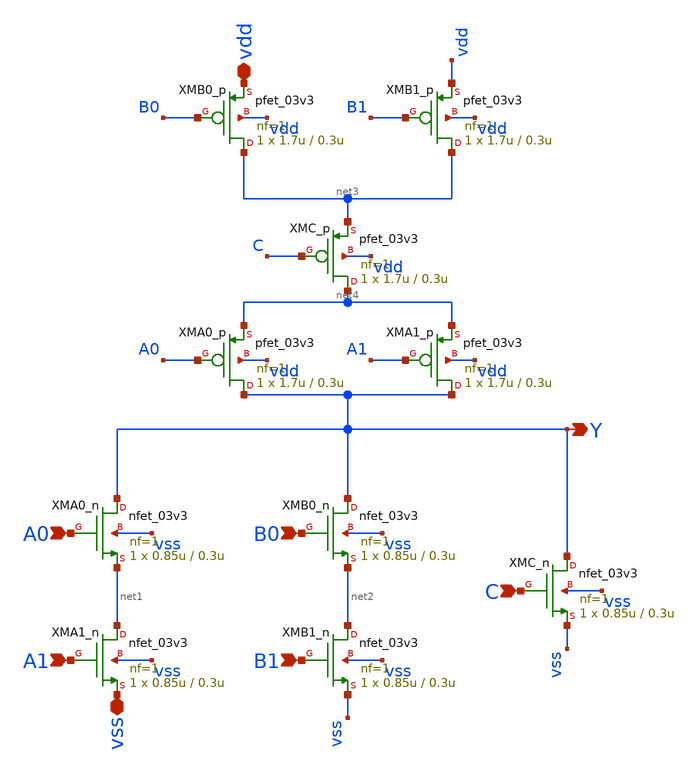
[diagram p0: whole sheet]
** sch_path: gf180mcu_osu_sc_gp9t3v3/xschem/gf180mcu_osu_sc_gp9t3v3__aoi221_1.sch
**.subckt gf180mcu_osu_sc_gp9t3v3__aoi221_1 vdd vss A0 A1 B1 B0 C Y
*.iopin vdd
*.iopin vss
*.ipin A0
*.ipin A1
*.ipin B1
*.ipin B0
*.ipin C
*.opin Y
XMA0_n Y A0 net1 vss nfet_03v3 L=0.3u W=0.85u nf=1 ad='int((nf+1)/2) * W/nf * 0.18u' as='int((nf+2)/2) * W/nf * 0.18u'
+ pd='2*int((nf+1)/2) * (W/nf + 0.18u)' ps='2*int((nf+2)/2) * (W/nf + 0.18u)' nrd='0.18u / W' nrs='0.18u / W'
+ sa=0 sb=0 sd=0 m=1
XMA1_n net1 A1 vss vss nfet_03v3 L=0.3u W=0.85u nf=1 ad='int((nf+1)/2) * W/nf * 0.18u' as='int((nf+2)/2) * W/nf * 0.18u'
+ pd='2*int((nf+1)/2) * (W/nf + 0.18u)' ps='2*int((nf+2)/2) * (W/nf + 0.18u)' nrd='0.18u / W' nrs='0.18u / W'
+ sa=0 sb=0 sd=0 m=1
XMB0_n Y B0 net2 vss nfet_03v3 L=0.3u W=0.85u nf=1 ad='int((nf+1)/2) * W/nf * 0.18u' as='int((nf+2)/2) * W/nf * 0.18u'
+ pd='2*int((nf+1)/2) * (W/nf + 0.18u)' ps='2*int((nf+2)/2) * (W/nf + 0.18u)' nrd='0.18u / W' nrs='0.18u / W'
+ sa=0 sb=0 sd=0 m=1
XMB1_n net2 B1 vss vss nfet_03v3 L=0.3u W=0.85u nf=1 ad='int((nf+1)/2) * W/nf * 0.18u' as='int((nf+2)/2) * W/nf * 0.18u'
+ pd='2*int((nf+1)/2) * (W/nf + 0.18u)' ps='2*int((nf+2)/2) * (W/nf + 0.18u)' nrd='0.18u / W' nrs='0.18u / W'
+ sa=0 sb=0 sd=0 m=1
XMC_n Y C vss vss nfet_03v3 L=0.3u W=0.85u nf=1 ad='int((nf+1)/2) * W/nf * 0.18u' as='int((nf+2)/2) * W/nf * 0.18u'
+ pd='2*int((nf+1)/2) * (W/nf + 0.18u)' ps='2*int((nf+2)/2) * (W/nf + 0.18u)' nrd='0.18u / W' nrs='0.18u / W'
+ sa=0 sb=0 sd=0 m=1
XMB0_p net3 B0 vdd vdd pfet_03v3 L=0.3u W=1.7u nf=1 ad='int((nf+1)/2) * W/nf * 0.18u' as='int((nf+2)/2) * W/nf * 0.18u'
+ pd='2*int((nf+1)/2) * (W/nf + 0.18u)' ps='2*int((nf+2)/2) * (W/nf + 0.18u)' nrd='0.18u / W' nrs='0.18u / W'
+ sa=0 sb=0 sd=0 m=1
XMB1_p net3 B1 vdd vdd pfet_03v3 L=0.3u W=1.7u nf=1 ad='int((nf+1)/2) * W/nf * 0.18u' as='int((nf+2)/2) * W/nf * 0.18u'
+ pd='2*int((nf+1)/2) * (W/nf + 0.18u)' ps='2*int((nf+2)/2) * (W/nf + 0.18u)' nrd='0.18u / W' nrs='0.18u / W'
+ sa=0 sb=0 sd=0 m=1
XMA0_p Y A0 net4 vdd pfet_03v3 L=0.3u W=1.7u nf=1 ad='int((nf+1)/2) * W/nf * 0.18u' as='int((nf+2)/2) * W/nf * 0.18u'
+ pd='2*int((nf+1)/2) * (W/nf + 0.18u)' ps='2*int((nf+2)/2) * (W/nf + 0.18u)' nrd='0.18u / W' nrs='0.18u / W'
+ sa=0 sb=0 sd=0 m=1
XMA1_p Y A1 net4 vdd pfet_03v3 L=0.3u W=1.7u nf=1 ad='int((nf+1)/2) * W/nf * 0.18u' as='int((nf+2)/2) * W/nf * 0.18u'
+ pd='2*int((nf+1)/2) * (W/nf + 0.18u)' ps='2*int((nf+2)/2) * (W/nf + 0.18u)' nrd='0.18u / W' nrs='0.18u / W'
+ sa=0 sb=0 sd=0 m=1
XMC_p net4 C net3 vdd pfet_03v3 L=0.3u W=1.7u nf=1 ad='int((nf+1)/2) * W/nf * 0.18u' as='int((nf+2)/2) * W/nf * 0.18u'
+ pd='2*int((nf+1)/2) * (W/nf + 0.18u)' ps='2*int((nf+2)/2) * (W/nf + 0.18u)' nrd='0.18u / W' nrs='0.18u / W'
+ sa=0 sb=0 sd=0 m=1
**.ends
.end
